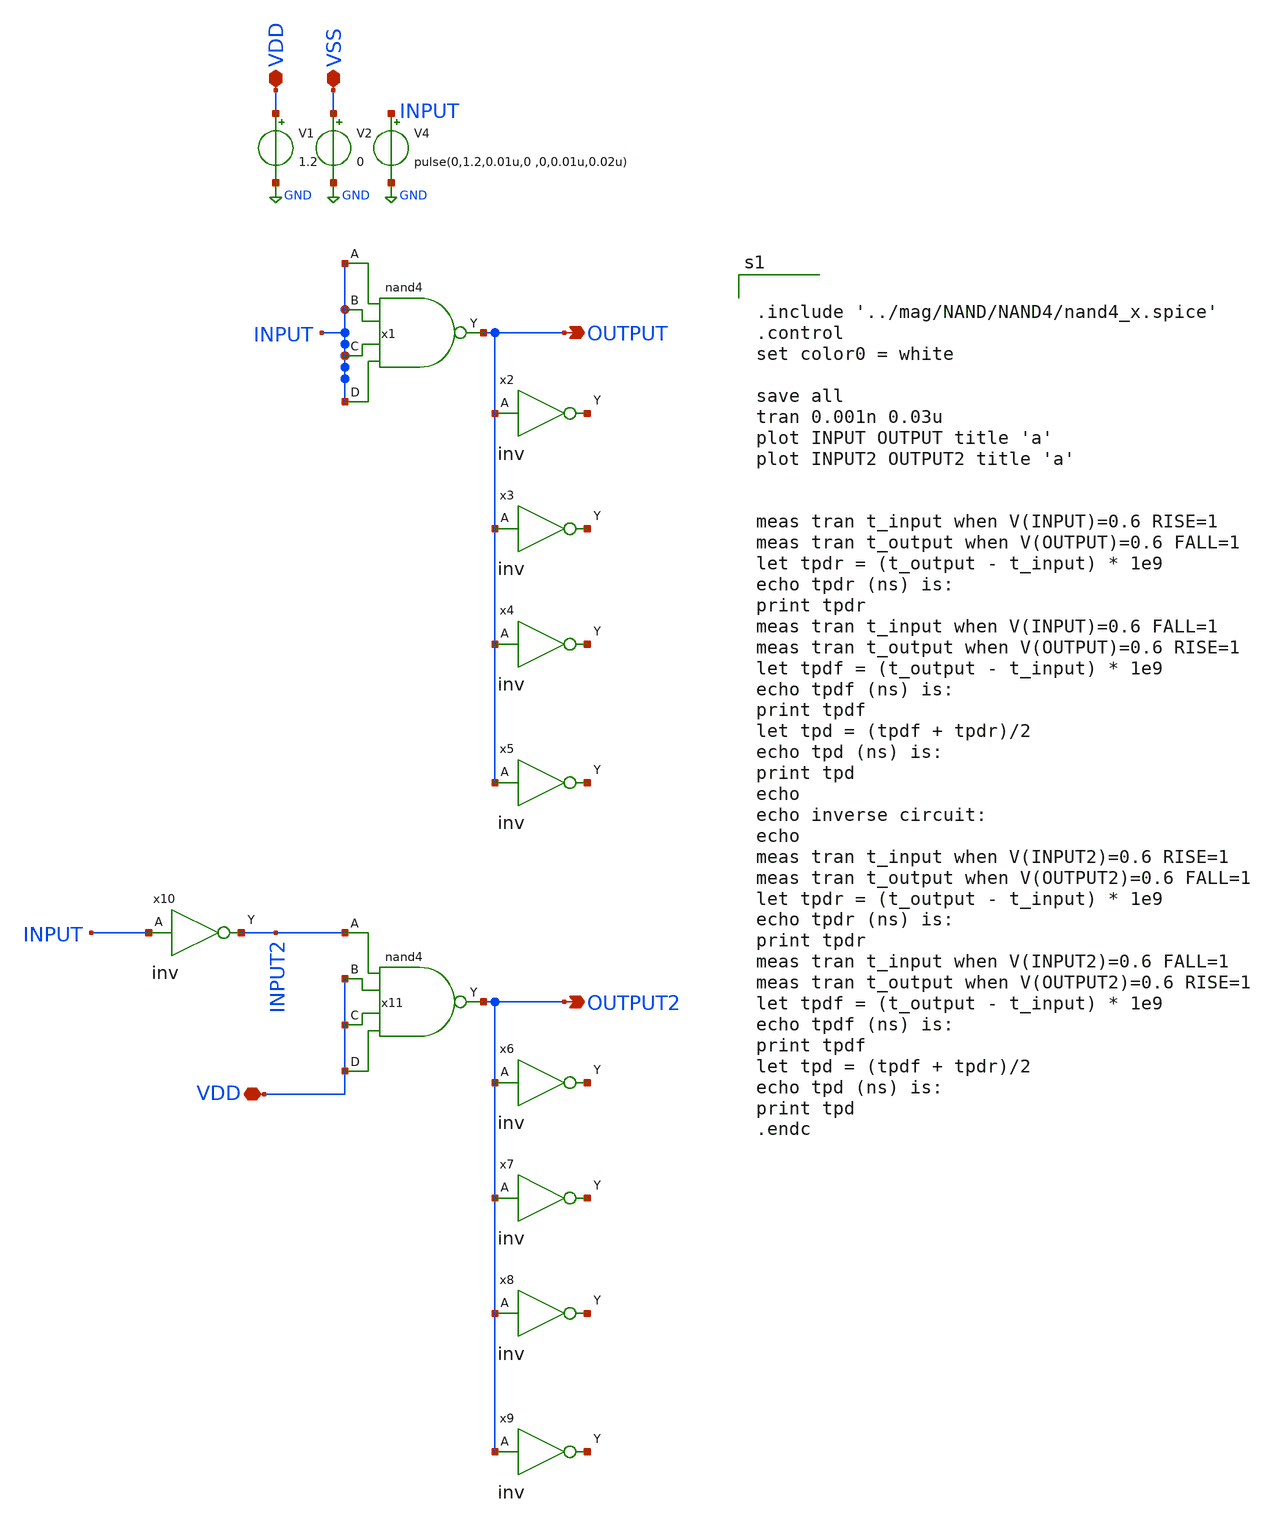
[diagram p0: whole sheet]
** sch_path: design/xschem/From Layout/NOR/nor4_TB.sch
**.subckt nor4_TB OUTPUT VDD VSS OUTPUT2 VDD
*.opin OUTPUT
*.iopin VDD
*.iopin VSS
*.opin OUTPUT2
*.iopin VDD
V1 VDD GND 1.2
V2 VSS GND 0
V4 INPUT GND pulse(0,1.2,0.01u,0 ,0,0.01u,0.02u)
x1 INPUT INPUT INPUT INPUT VSS VDD OUTPUT nand4
x2 OUTPUT VSS VDD net1 inv
x3 OUTPUT VSS VDD net2 inv
x4 OUTPUT VSS VDD net3 inv
x5 OUTPUT VSS VDD net4 inv
x6 OUTPUT2 VSS VDD net5 inv
x7 OUTPUT2 VSS VDD net6 inv
x8 OUTPUT2 VSS VDD net7 inv
x9 OUTPUT2 VSS VDD net8 inv
x10 INPUT VSS VDD INPUT2 inv
x11 INPUT2 VDD VDD VDD VSS VDD OUTPUT2 nand4
**** begin user architecture code

** opencircuitdesign pdks install
.lib $::SKYWATER_MODELS/sky130.lib.spice tt_mm




.include '../mag/NAND/NAND4/nand4_x.spice'
.control
set color0 = white

save all
tran 0.001n 0.03u
plot INPUT OUTPUT title 'a'
plot INPUT2 OUTPUT2 title 'a'


meas tran t_input when V(INPUT)=0.6 RISE=1
meas tran t_output when V(OUTPUT)=0.6 FALL=1
let tpdr = (t_output - t_input) * 1e9
echo tpdr (ns) is:
print tpdr
meas tran t_input when V(INPUT)=0.6 FALL=1
meas tran t_output when V(OUTPUT)=0.6 RISE=1
let tpdf = (t_output - t_input) * 1e9
echo tpdf (ns) is:
print tpdf
let tpd = (tpdf + tpdr)/2
echo tpd (ns) is:
print tpd
echo
echo inverse circuit:
echo
meas tran t_input when V(INPUT2)=0.6 RISE=1
meas tran t_output when V(OUTPUT2)=0.6 FALL=1
let tpdr = (t_output - t_input) * 1e9
echo tpdr (ns) is:
print tpdr
meas tran t_input when V(INPUT2)=0.6 FALL=1
meas tran t_output when V(OUTPUT2)=0.6 RISE=1
let tpdf = (t_output - t_input) * 1e9
echo tpdf (ns) is:
print tpdf
let tpd = (tpdf + tpdr)/2
echo tpd (ns) is:
print tpd
.endc


**** end user architecture code
**.ends
.GLOBAL GND
.end
